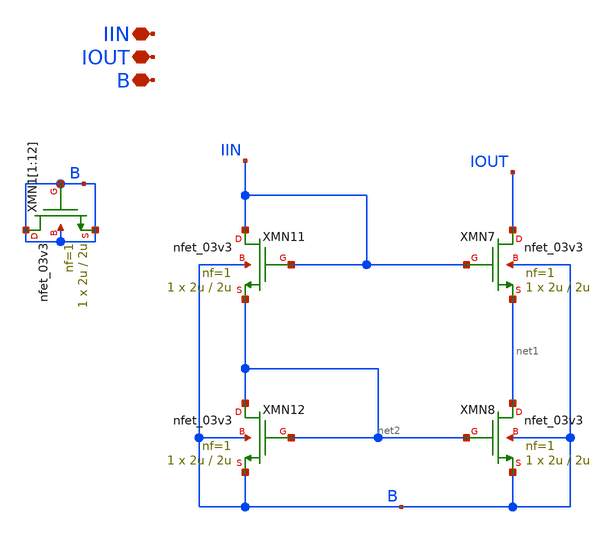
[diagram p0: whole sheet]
** sch_path: Voltage_Reference/symbols_vr/CM_in.sch
**.subckt CM_in IIN IOUT B
*.iopin IIN
*.iopin IOUT
*.iopin B
XMN7 IOUT IIN net1 B nfet_03v3 L=2u W=2u nf=1 ad='int((nf+1)/2) * W/nf * 0.18u' as='int((nf+2)/2) * W/nf * 0.18u'
+ pd='2*int((nf+1)/2) * (W/nf + 0.18u)' ps='2*int((nf+2)/2) * (W/nf + 0.18u)' nrd='0.18u / W' nrs='0.18u / W'
+ sa=0 sb=0 sd=0 m=1
XMN8 net1 net2 B B nfet_03v3 L=2u W=2u nf=1 ad='int((nf+1)/2) * W/nf * 0.18u' as='int((nf+2)/2) * W/nf * 0.18u'
+ pd='2*int((nf+1)/2) * (W/nf + 0.18u)' ps='2*int((nf+2)/2) * (W/nf + 0.18u)' nrd='0.18u / W' nrs='0.18u / W'
+ sa=0 sb=0 sd=0 m=1
XMN11 IIN IIN net2 B nfet_03v3 L=2u W=2u nf=1 ad='int((nf+1)/2) * W/nf * 0.18u' as='int((nf+2)/2) * W/nf * 0.18u'
+ pd='2*int((nf+1)/2) * (W/nf + 0.18u)' ps='2*int((nf+2)/2) * (W/nf + 0.18u)' nrd='0.18u / W' nrs='0.18u / W'
+ sa=0 sb=0 sd=0 m=1
XMN12 net2 net2 B B nfet_03v3 L=2u W=2u nf=1 ad='int((nf+1)/2) * W/nf * 0.18u' as='int((nf+2)/2) * W/nf * 0.18u'
+ pd='2*int((nf+1)/2) * (W/nf + 0.18u)' ps='2*int((nf+2)/2) * (W/nf + 0.18u)' nrd='0.18u / W' nrs='0.18u / W'
+ sa=0 sb=0 sd=0 m=1
XMN1[1] B B B B nfet_03v3 L=2u W=2u nf=1 ad='int((nf+1)/2) * W/nf * 0.18u' as='int((nf+2)/2) * W/nf * 0.18u'
+ pd='2*int((nf+1)/2) * (W/nf + 0.18u)' ps='2*int((nf+2)/2) * (W/nf + 0.18u)' nrd='0.18u / W' nrs='0.18u / W'
+ sa=0 sb=0 sd=0 m=1
XMN1[2] B B B B nfet_03v3 L=2u W=2u nf=1 ad='int((nf+1)/2) * W/nf * 0.18u' as='int((nf+2)/2) * W/nf * 0.18u'
+ pd='2*int((nf+1)/2) * (W/nf + 0.18u)' ps='2*int((nf+2)/2) * (W/nf + 0.18u)' nrd='0.18u / W' nrs='0.18u / W'
+ sa=0 sb=0 sd=0 m=1
XMN1[3] B B B B nfet_03v3 L=2u W=2u nf=1 ad='int((nf+1)/2) * W/nf * 0.18u' as='int((nf+2)/2) * W/nf * 0.18u'
+ pd='2*int((nf+1)/2) * (W/nf + 0.18u)' ps='2*int((nf+2)/2) * (W/nf + 0.18u)' nrd='0.18u / W' nrs='0.18u / W'
+ sa=0 sb=0 sd=0 m=1
XMN1[4] B B B B nfet_03v3 L=2u W=2u nf=1 ad='int((nf+1)/2) * W/nf * 0.18u' as='int((nf+2)/2) * W/nf * 0.18u'
+ pd='2*int((nf+1)/2) * (W/nf + 0.18u)' ps='2*int((nf+2)/2) * (W/nf + 0.18u)' nrd='0.18u / W' nrs='0.18u / W'
+ sa=0 sb=0 sd=0 m=1
XMN1[5] B B B B nfet_03v3 L=2u W=2u nf=1 ad='int((nf+1)/2) * W/nf * 0.18u' as='int((nf+2)/2) * W/nf * 0.18u'
+ pd='2*int((nf+1)/2) * (W/nf + 0.18u)' ps='2*int((nf+2)/2) * (W/nf + 0.18u)' nrd='0.18u / W' nrs='0.18u / W'
+ sa=0 sb=0 sd=0 m=1
XMN1[6] B B B B nfet_03v3 L=2u W=2u nf=1 ad='int((nf+1)/2) * W/nf * 0.18u' as='int((nf+2)/2) * W/nf * 0.18u'
+ pd='2*int((nf+1)/2) * (W/nf + 0.18u)' ps='2*int((nf+2)/2) * (W/nf + 0.18u)' nrd='0.18u / W' nrs='0.18u / W'
+ sa=0 sb=0 sd=0 m=1
XMN1[7] B B B B nfet_03v3 L=2u W=2u nf=1 ad='int((nf+1)/2) * W/nf * 0.18u' as='int((nf+2)/2) * W/nf * 0.18u'
+ pd='2*int((nf+1)/2) * (W/nf + 0.18u)' ps='2*int((nf+2)/2) * (W/nf + 0.18u)' nrd='0.18u / W' nrs='0.18u / W'
+ sa=0 sb=0 sd=0 m=1
XMN1[8] B B B B nfet_03v3 L=2u W=2u nf=1 ad='int((nf+1)/2) * W/nf * 0.18u' as='int((nf+2)/2) * W/nf * 0.18u'
+ pd='2*int((nf+1)/2) * (W/nf + 0.18u)' ps='2*int((nf+2)/2) * (W/nf + 0.18u)' nrd='0.18u / W' nrs='0.18u / W'
+ sa=0 sb=0 sd=0 m=1
XMN1[9] B B B B nfet_03v3 L=2u W=2u nf=1 ad='int((nf+1)/2) * W/nf * 0.18u' as='int((nf+2)/2) * W/nf * 0.18u'
+ pd='2*int((nf+1)/2) * (W/nf + 0.18u)' ps='2*int((nf+2)/2) * (W/nf + 0.18u)' nrd='0.18u / W' nrs='0.18u / W'
+ sa=0 sb=0 sd=0 m=1
XMN1[10] B B B B nfet_03v3 L=2u W=2u nf=1 ad='int((nf+1)/2) * W/nf * 0.18u' as='int((nf+2)/2) * W/nf * 0.18u'
+ pd='2*int((nf+1)/2) * (W/nf + 0.18u)' ps='2*int((nf+2)/2) * (W/nf + 0.18u)' nrd='0.18u / W' nrs='0.18u / W'
+ sa=0 sb=0 sd=0 m=1
XMN1[11] B B B B nfet_03v3 L=2u W=2u nf=1 ad='int((nf+1)/2) * W/nf * 0.18u' as='int((nf+2)/2) * W/nf * 0.18u'
+ pd='2*int((nf+1)/2) * (W/nf + 0.18u)' ps='2*int((nf+2)/2) * (W/nf + 0.18u)' nrd='0.18u / W' nrs='0.18u / W'
+ sa=0 sb=0 sd=0 m=1
XMN1[12] B B B B nfet_03v3 L=2u W=2u nf=1 ad='int((nf+1)/2) * W/nf * 0.18u' as='int((nf+2)/2) * W/nf * 0.18u'
+ pd='2*int((nf+1)/2) * (W/nf + 0.18u)' ps='2*int((nf+2)/2) * (W/nf + 0.18u)' nrd='0.18u / W' nrs='0.18u / W'
+ sa=0 sb=0 sd=0 m=1
**.ends
.end
